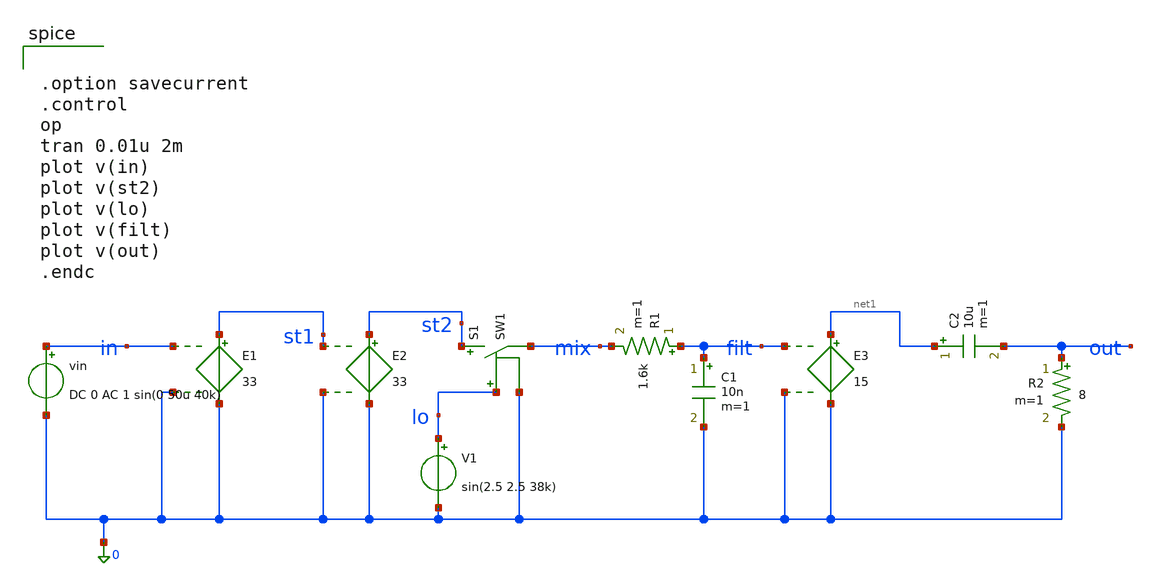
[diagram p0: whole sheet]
** sch_path: member_project/JJY_Receiver/Masahiro/jjy_recv/system_sim/system_sim.sch
**.subckt system_sim
E1 st1 0 in 0 33
vin in 0 DC 0 AC 1 sin(0 50u 40k)
E2 st2 0 st1 0 33
S1 st2 mix lo 0 SW1
V1 lo 0 sin(2.5 2.5 38k)
R1 filt mix 1.6k m=1
C1 filt 0 10n m=1
R2 out 0 8 m=1
C2 net1 out 10u m=1
E3 net1 0 filt 0 15
**** begin user architecture code


.option savecurrent
.control
op
tran 0.01u 2m
plot v(in)
plot v(st2)
plot v(lo)
plot v(filt)
plot v(out)
.endc


**** end user architecture code
**.ends
**** begin user architecture code
.MODEL SW1 SW   VT=2.5 VH=0.01  RON=0.01 ROFF=10G
**** end user architecture code
.end
